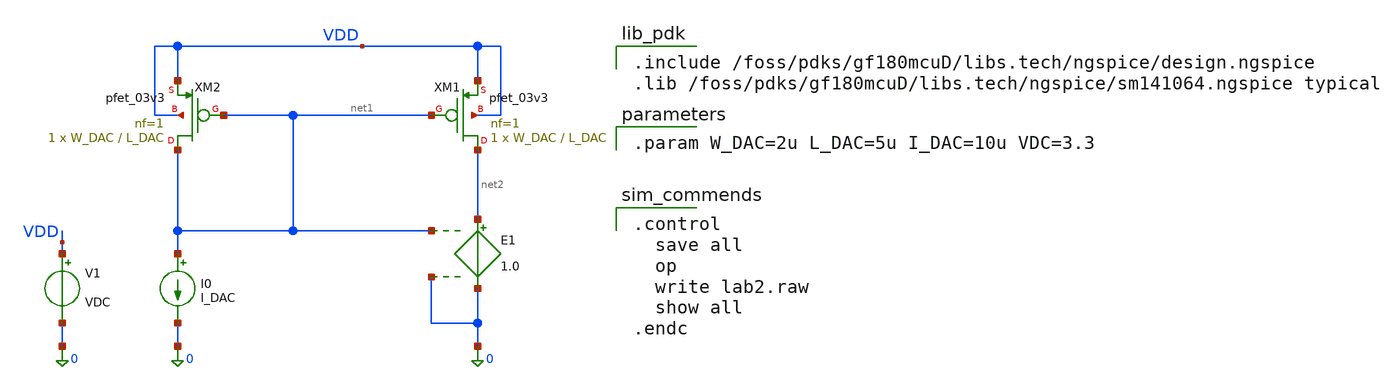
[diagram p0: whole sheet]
** sch_path: lab_2/lab2.sch
**.subckt lab2
I0 net1 0 I_DAC
E1 net2 0 net1 0 1.0
V1 VDD 0 VDC
XM1 net2 net1 VDD VDD pfet_03v3 L=L_DAC W=W_DAC nf=1 ad='int((nf+1)/2) * W/nf * 0.18u' as='int((nf+2)/2) * W/nf * 0.18u'
+ pd='2*int((nf+1)/2) * (W/nf + 0.18u)' ps='2*int((nf+2)/2) * (W/nf + 0.18u)' nrd='0.18u / W' nrs='0.18u / W'
+ sa=0 sb=0 sd=0 m=1
XM2 net1 net1 VDD VDD pfet_03v3 L=L_DAC W=W_DAC nf=1 ad='int((nf+1)/2) * W/nf * 0.18u' as='int((nf+2)/2) * W/nf * 0.18u'
+ pd='2*int((nf+1)/2) * (W/nf + 0.18u)' ps='2*int((nf+2)/2) * (W/nf + 0.18u)' nrd='0.18u / W' nrs='0.18u / W'
+ sa=0 sb=0 sd=0 m=1
**** begin user architecture code

.include /foss/pdks/gf180mcuD/libs.tech/ngspice/design.ngspice
.lib /foss/pdks/gf180mcuD/libs.tech/ngspice/sm141064.ngspice typical


.param W_DAC=2u L_DAC=5u I_DAC=10u VDC=3.3


.control
  save all
  op
  write lab2.raw
  show all
.endc

**** end user architecture code
**.ends
.end
